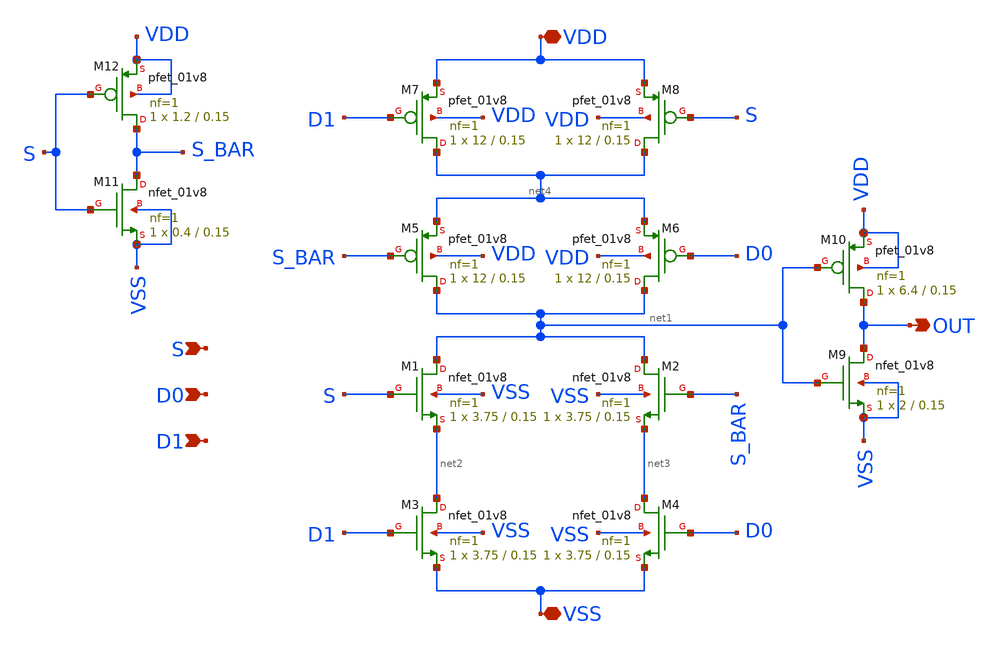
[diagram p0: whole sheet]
** sch_path: design/2x1_mux_with_fo4/2x1_mux.sch
**.subckt 2x1_mux VSS VDD S D0 D1 OUT
*.iopin VSS
*.iopin VDD
*.ipin S
*.ipin D0
*.ipin D1
*.opin OUT
XM2 net1 S_BAR net3 VSS sky130_fd_pr__nfet_01v8 L=0.15 W=3.75 nf=1 ad='int((nf+1)/2) * W/nf * 0.29' as='int((nf+2)/2) * W/nf * 0.29'
+ pd='2*int((nf+1)/2) * (W/nf + 0.29)' ps='2*int((nf+2)/2) * (W/nf + 0.29)' nrd='0.29 / W' nrs='0.29 / W'
+ sa=0 sb=0 sd=0 mult=1 m=1
XM3 net2 D1 VSS VSS sky130_fd_pr__nfet_01v8 L=0.15 W=3.75 nf=1 ad='int((nf+1)/2) * W/nf * 0.29' as='int((nf+2)/2) * W/nf * 0.29'
+ pd='2*int((nf+1)/2) * (W/nf + 0.29)' ps='2*int((nf+2)/2) * (W/nf + 0.29)' nrd='0.29 / W' nrs='0.29 / W'
+ sa=0 sb=0 sd=0 mult=1 m=1
XM4 net3 D0 VSS VSS sky130_fd_pr__nfet_01v8 L=0.15 W=3.75 nf=1 ad='int((nf+1)/2) * W/nf * 0.29' as='int((nf+2)/2) * W/nf * 0.29'
+ pd='2*int((nf+1)/2) * (W/nf + 0.29)' ps='2*int((nf+2)/2) * (W/nf + 0.29)' nrd='0.29 / W' nrs='0.29 / W'
+ sa=0 sb=0 sd=0 mult=1 m=1
XM5 net1 S_BAR net4 VDD sky130_fd_pr__pfet_01v8 L=0.15 W=12 nf=1 ad='int((nf+1)/2) * W/nf * 0.29' as='int((nf+2)/2) * W/nf * 0.29'
+ pd='2*int((nf+1)/2) * (W/nf + 0.29)' ps='2*int((nf+2)/2) * (W/nf + 0.29)' nrd='0.29 / W' nrs='0.29 / W'
+ sa=0 sb=0 sd=0 mult=1 m=1
XM7 net4 D1 VDD VDD sky130_fd_pr__pfet_01v8 L=0.15 W=12 nf=1 ad='int((nf+1)/2) * W/nf * 0.29' as='int((nf+2)/2) * W/nf * 0.29'
+ pd='2*int((nf+1)/2) * (W/nf + 0.29)' ps='2*int((nf+2)/2) * (W/nf + 0.29)' nrd='0.29 / W' nrs='0.29 / W'
+ sa=0 sb=0 sd=0 mult=1 m=1
XM8 net4 S VDD VDD sky130_fd_pr__pfet_01v8 L=0.15 W=12 nf=1 ad='int((nf+1)/2) * W/nf * 0.29' as='int((nf+2)/2) * W/nf * 0.29'
+ pd='2*int((nf+1)/2) * (W/nf + 0.29)' ps='2*int((nf+2)/2) * (W/nf + 0.29)' nrd='0.29 / W' nrs='0.29 / W'
+ sa=0 sb=0 sd=0 mult=1 m=1
XM9 OUT net1 VSS VSS sky130_fd_pr__nfet_01v8 L=0.15 W=2 nf=1 ad='int((nf+1)/2) * W/nf * 0.29' as='int((nf+2)/2) * W/nf * 0.29'
+ pd='2*int((nf+1)/2) * (W/nf + 0.29)' ps='2*int((nf+2)/2) * (W/nf + 0.29)' nrd='0.29 / W' nrs='0.29 / W'
+ sa=0 sb=0 sd=0 mult=1 m=1
XM10 OUT net1 VDD VDD sky130_fd_pr__pfet_01v8 L=0.15 W=6.4 nf=1 ad='int((nf+1)/2) * W/nf * 0.29' as='int((nf+2)/2) * W/nf * 0.29'
+ pd='2*int((nf+1)/2) * (W/nf + 0.29)' ps='2*int((nf+2)/2) * (W/nf + 0.29)' nrd='0.29 / W' nrs='0.29 / W'
+ sa=0 sb=0 sd=0 mult=1 m=1
XM12 S_BAR S VDD VDD sky130_fd_pr__pfet_01v8 L=0.15 W=1.2 nf=1 ad='int((nf+1)/2) * W/nf * 0.29' as='int((nf+2)/2) * W/nf * 0.29'
+ pd='2*int((nf+1)/2) * (W/nf + 0.29)' ps='2*int((nf+2)/2) * (W/nf + 0.29)' nrd='0.29 / W' nrs='0.29 / W'
+ sa=0 sb=0 sd=0 mult=1 m=1
XM11 S_BAR S VSS VSS sky130_fd_pr__nfet_01v8 L=0.15 W=0.4 nf=1 ad='int((nf+1)/2) * W/nf * 0.29' as='int((nf+2)/2) * W/nf * 0.29'
+ pd='2*int((nf+1)/2) * (W/nf + 0.29)' ps='2*int((nf+2)/2) * (W/nf + 0.29)' nrd='0.29 / W' nrs='0.29 / W'
+ sa=0 sb=0 sd=0 mult=1 m=1
XM1 net1 S net2 VSS sky130_fd_pr__nfet_01v8 L=0.15 W=3.75 nf=1 ad='int((nf+1)/2) * W/nf * 0.29' as='int((nf+2)/2) * W/nf * 0.29'
+ pd='2*int((nf+1)/2) * (W/nf + 0.29)' ps='2*int((nf+2)/2) * (W/nf + 0.29)' nrd='0.29 / W' nrs='0.29 / W'
+ sa=0 sb=0 sd=0 mult=1 m=1
XM6 net1 D0 net4 VDD sky130_fd_pr__pfet_01v8 L=0.15 W=12 nf=1 ad='int((nf+1)/2) * W/nf * 0.29' as='int((nf+2)/2) * W/nf * 0.29'
+ pd='2*int((nf+1)/2) * (W/nf + 0.29)' ps='2*int((nf+2)/2) * (W/nf + 0.29)' nrd='0.29 / W' nrs='0.29 / W'
+ sa=0 sb=0 sd=0 mult=1 m=1
**.ends
.end
